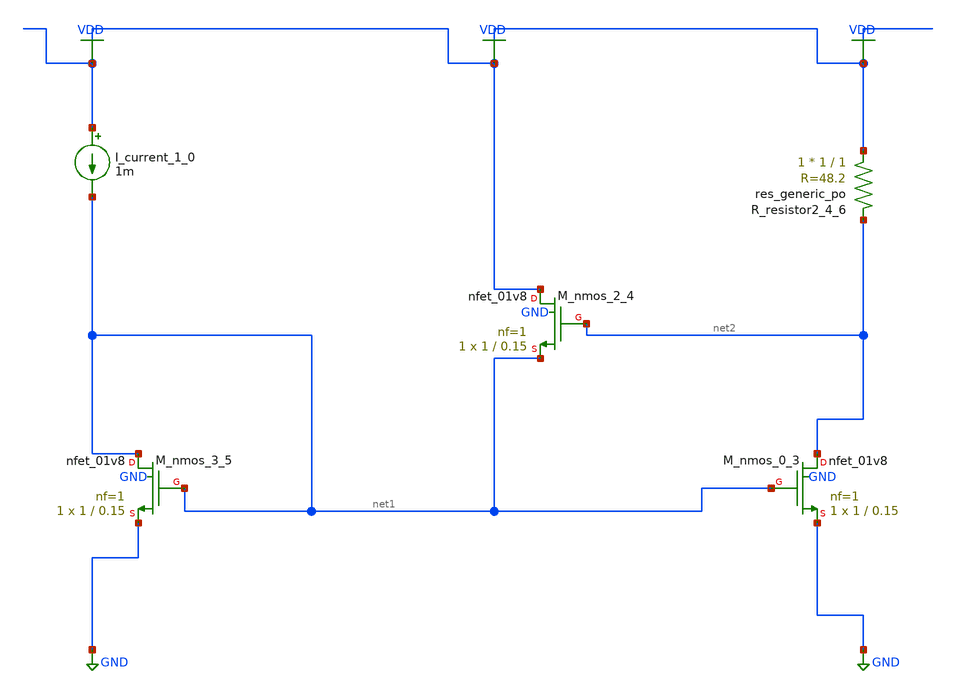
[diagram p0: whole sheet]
** sch_path: schematics/AMSNet/334.sch
**.subckt 334
I_current_1_0 VDD net1 1m
XM_nmos_0_3 net2 net1 GND GND sky130_fd_pr__nfet_01v8 L=0.15 W=1 nf=1 ad='int((1 + 1)/2) * 1 / 1 * 0.29'
+ as='int((1 + 2)/2) * 1 / 1 * 0.29' pd='2*int((1 + 1)/2) * (1 / 1 + 0.29)' ps='2*int((1 + 2)/2) * (1 / 1 + 0.29)'
+ nrd='0.29 / 1 ' nrs='0.29 / 1 ' sa=0 sb=0 sd=0 mult=1 m=1
XM_nmos_2_4 VDD net2 net1 GND sky130_fd_pr__nfet_01v8 L=0.15 W=1 nf=1 ad='int((1 + 1)/2) * 1 / 1 * 0.29'
+ as='int((1 + 2)/2) * 1 / 1 * 0.29' pd='2*int((1 + 1)/2) * (1 / 1 + 0.29)' ps='2*int((1 + 2)/2) * (1 / 1 + 0.29)'
+ nrd='0.29 / 1 ' nrs='0.29 / 1 ' sa=0 sb=0 sd=0 mult=1 m=1
XM_nmos_3_5 net1 net1 GND GND sky130_fd_pr__nfet_01v8 L=0.15 W=1 nf=1 ad='int((1 + 1)/2) * 1 / 1 * 0.29'
+ as='int((1 + 2)/2) * 1 / 1 * 0.29' pd='2*int((1 + 1)/2) * (1 / 1 + 0.29)' ps='2*int((1 + 2)/2) * (1 / 1 + 0.29)'
+ nrd='0.29 / 1 ' nrs='0.29 / 1 ' sa=0 sb=0 sd=0 mult=1 m=1
XR_resistor2_4_6 VDD net2 sky130_fd_pr__res_generic_po W=1 L=1 m=1
**.ends
.GLOBAL GND
.GLOBAL VDD
.end
